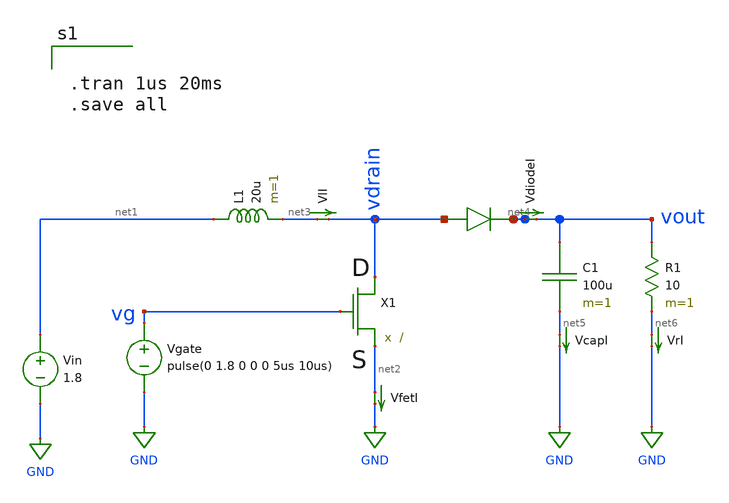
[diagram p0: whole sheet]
** sch_path: schematics/simple_boost_circuit.sch
**.subckt simple_boost_circuit
Vin net1 GND 1.8
VfetI net2 GND 0
.save i(vfeti)
X1 vdrain vg net2 power_nfet
Vgate vg GND pulse(0 1.8 0 0 0 5us 10us)
L1 net1 net3 20u m=1
D1 vdrain net4 diode_schottky
C1 vout net5 100u m=1
R1 vout net6 10 m=1
VlI net3 vdrain 0
.save i(vli)
VdiodeI net4 vout 0
.save i(vdiodei)
VcapI net5 GND 0
.save i(vcapi)
VrI net6 GND 0
.save i(vri)
**** begin user architecture code


.tran 1us 20ms
.save all



*SRC=DMN2009LSS;DI_DMN2009LSS;MOSFETs N;Enh;20.0V 12.0A 8.00mohms  Diodes Inc. MOSFET
*SYM=POWMOSN
.SUBCKT power_nfet 10 20 30
*     TERMINALS:  D  G  S
M1   1  2  3  3  DMOS L=1U W=1U
RD  10  1  2.80m
RS  40  3  1.20m
RG  20  2  12.5
CGS  2  3  2.46n
EGD 12  0  2  1  1
VFB 14  0  0
FFB  2  1  VFB  1
CGD 13 14  663p
R1  13  0  1.00
D1  12 13  DLIM
DDG 15 14  DCGD
R2  12 15  1.00
D2  15  0  DLIM
DSD  3 10  DSUB
LS  30 40  7.50n
.model DMOS NMOS(LEVEL=3 VMAX=41.7k THETA=60.0m  ETA=2.00m VTO=1 KP=274
.model DCGD D (CJO=663p VJ=0.600 M=0.680
.model DSUB D (IS=49.8n N=1.50 RS=37.5m BV=20.0  CJO=1.28n VJ=0.800 M=0.420 TT=297n
.model DLIM D (IS=100U)
.ends



*SRC=SBR10U40CT;DI_SBR10U40CT;Diodes;Si;  40.0V  5.00A  35.0ns   Diodes INC SBR rectifier
.model diode_schottky d ( IS=6.83m RS=6.69u BV=40.0 IBV=0.100 CJO=593p  M=0.333 N=7.19 TT=50.4n )

**** end user architecture code
**.ends
.GLOBAL GND
.end
